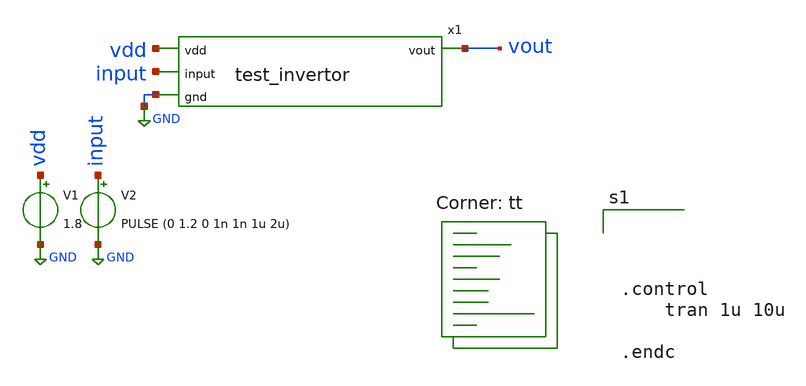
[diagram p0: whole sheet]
** sch_path: analog/schematics/test_invertor_tb.sch
**.subckt test_invertor_tb
V1 vdd GND 1.8
V2 input GND PULSE (0 1.2 0 1n 1n 1u 2u)
x1 vdd input vout GND test_invertor
**** begin user architecture code
.lib $::SKYWATER_MODELS/sky130.lib.spice tt




.control
	tran 1u 10u

.endc





**** end user architecture code
**.ends

* expanding   symbol:  test_invertor.sym # of pins=4
** sym_path: analog/schematics/test_invertor.sym
** sch_path: analog/schematics/test_invertor.sch
.subckt test_invertor vdd input vout gnd
*.ipin input
*.ipin gnd
*.ipin vdd
*.opin vout
XM1 vout input gnd gnd sky130_fd_pr__nfet_01v8 L=0.15 W=1 nf=1 ad='int((nf+1)/2) * W/nf * 0.29' as='int((nf+2)/2) * W/nf * 0.29'
+ pd='2*int((nf+1)/2) * (W/nf + 0.29)' ps='2*int((nf+2)/2) * (W/nf + 0.29)' nrd='0.29 / W' nrs='0.29 / W'
+ sa=0 sb=0 sd=0 mult=1 m=1
XM2 vout input vdd vdd sky130_fd_pr__pfet_01v8 L=0.15 W=1 nf=1 ad='int((nf+1)/2) * W/nf * 0.29' as='int((nf+2)/2) * W/nf * 0.29'
+ pd='2*int((nf+1)/2) * (W/nf + 0.29)' ps='2*int((nf+2)/2) * (W/nf + 0.29)' nrd='0.29 / W' nrs='0.29 / W'
+ sa=0 sb=0 sd=0 mult=1 m=1
.ends

.GLOBAL GND
.end
